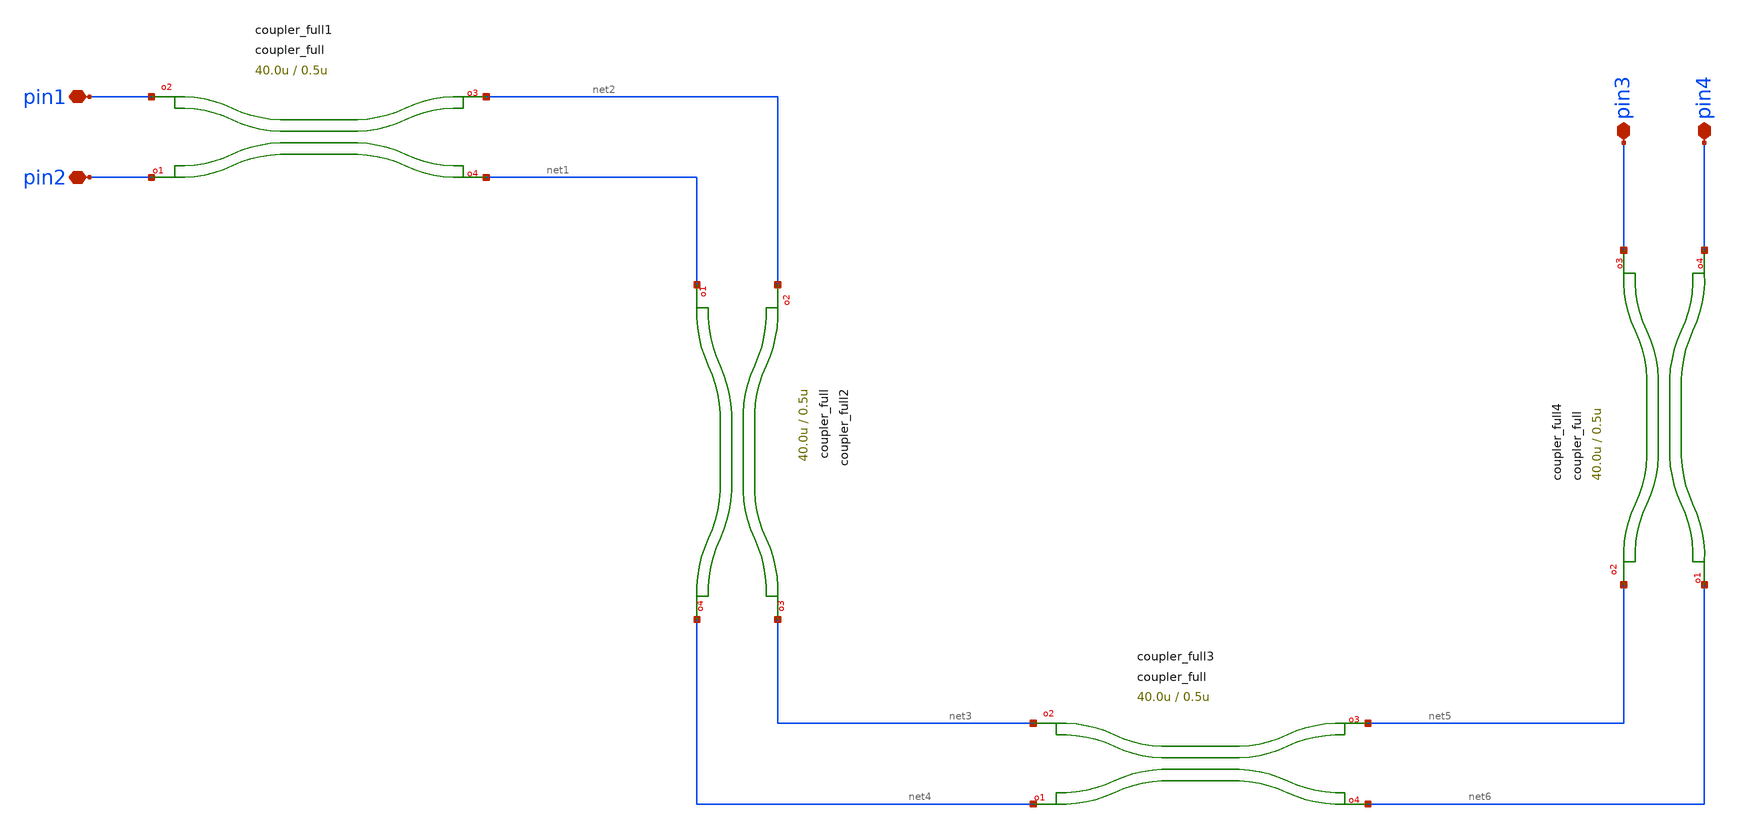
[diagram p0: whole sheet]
** sch_path: xschem/tests/test_sch/test_coupler_full.sch
* Copyright (c) 2024, Mabrains LLC
* Licensed under the GNU Lesser General Public License, Version 3.0 (the "License");
* you may not use this file except in compliance with the License.
* GNU Lesser General Public License
* Version 3, 29 June 2007
* This program is free software: you can redistribute it and/or modify
* it under the terms of the GNU Lesser General Public License as published
* by the Free Software Foundation, either version 3 of the License, or
* (at your option) any later version.
* This program is distributed in the hope that it will be useful,
* but WITHOUT ANY WARRANTY; without even the implied warranty of
* MERCHANTABILITY or FITNESS FOR A PARTICULAR PURPOSE.  See the
* GNU Lesser General Public License for more details.
* You should have received a copy of the GNU Lesser General Public License
* along with this program.  If not, see <https://www.gnu.org/licenses/>.
* SPDX-License-Identifier: LGPL-3.0
**.subckt test_coupler_full pin2 pin1 pin3 pin4
*.iopin pin2
*.iopin pin1
*.iopin pin3
*.iopin pin4
Pcoupler_full1 pin1 pin2 net2 net1 coupler_full coupling_length=40.0u dx=10.0u dy=4.8u gap=0.5u
+ dw=0.1u
Pcoupler_full3 net3 net4 net5 net6 coupler_full coupling_length=40.0u dx=10.0u dy=4.8u gap=0.5u
+ dw=0.1u
Pcoupler_full4 net5 net6 pin3 pin4 coupler_full coupling_length=40.0u dx=10.0u dy=4.8u gap=0.5u
+ dw=0.1u
Pcoupler_full2 net2 net1 net3 net4 coupler_full coupling_length=40.0u dx=10.0u dy=4.8u gap=0.5u
+ dw=0.1u
**.ends
.end
